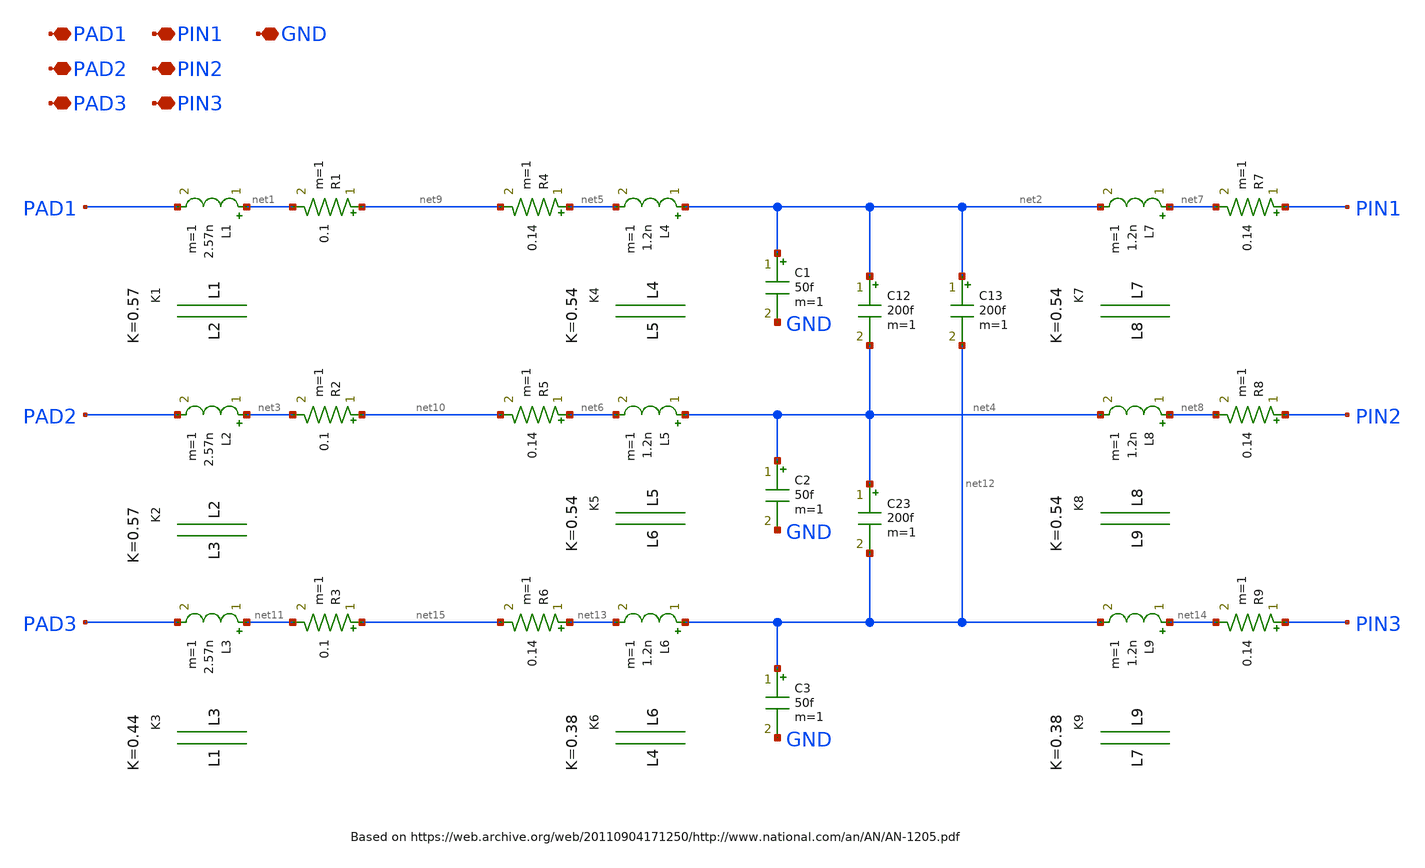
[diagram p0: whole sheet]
** sch_path: xschem/package_model.sch
**.subckt package_model PAD1 PAD2 PIN1 PIN2 GND PAD3 PIN3
*.iopin PAD1
*.iopin PAD2
*.iopin PIN1
*.iopin PIN2
*.iopin GND
*.iopin PAD3
*.iopin PIN3
R1 net9 net1 0.1 m=1
L1 net1 PAD1 2.57n m=1
C1 net2 GND 50f m=1
C12 net2 net4 200f m=1
K1 L1 L2 0.57
R2 net10 net3 0.1 m=1
L2 net3 PAD2 2.57n m=1
C2 net4 GND 50f m=1
R4 net5 net9 0.14 m=1
R5 net6 net10 0.14 m=1
L4 net2 net5 1.2n m=1
K4 L4 L5 0.54
L5 net4 net6 1.2n m=1
L7 net7 net2 1.2n m=1
K7 L7 L8 0.54
L8 net8 net4 1.2n m=1
R7 PIN1 net7 0.14 m=1
R8 PIN2 net8 0.14 m=1
R3 net15 net11 0.1 m=1
L3 net11 PAD3 2.57n m=1
C3 net12 GND 50f m=1
R6 net13 net15 0.14 m=1
L6 net12 net13 1.2n m=1
L9 net14 net12 1.2n m=1
R9 PIN3 net14 0.14 m=1
K2 L2 L3 0.57
K3 L3 L1 0.44
K5 L5 L6 0.54
K6 L6 L4 0.38
C23 net4 net12 200f m=1
C13 net2 net12 200f m=1
K8 L8 L9 0.54
K9 L9 L7 0.38
**.ends
.end
